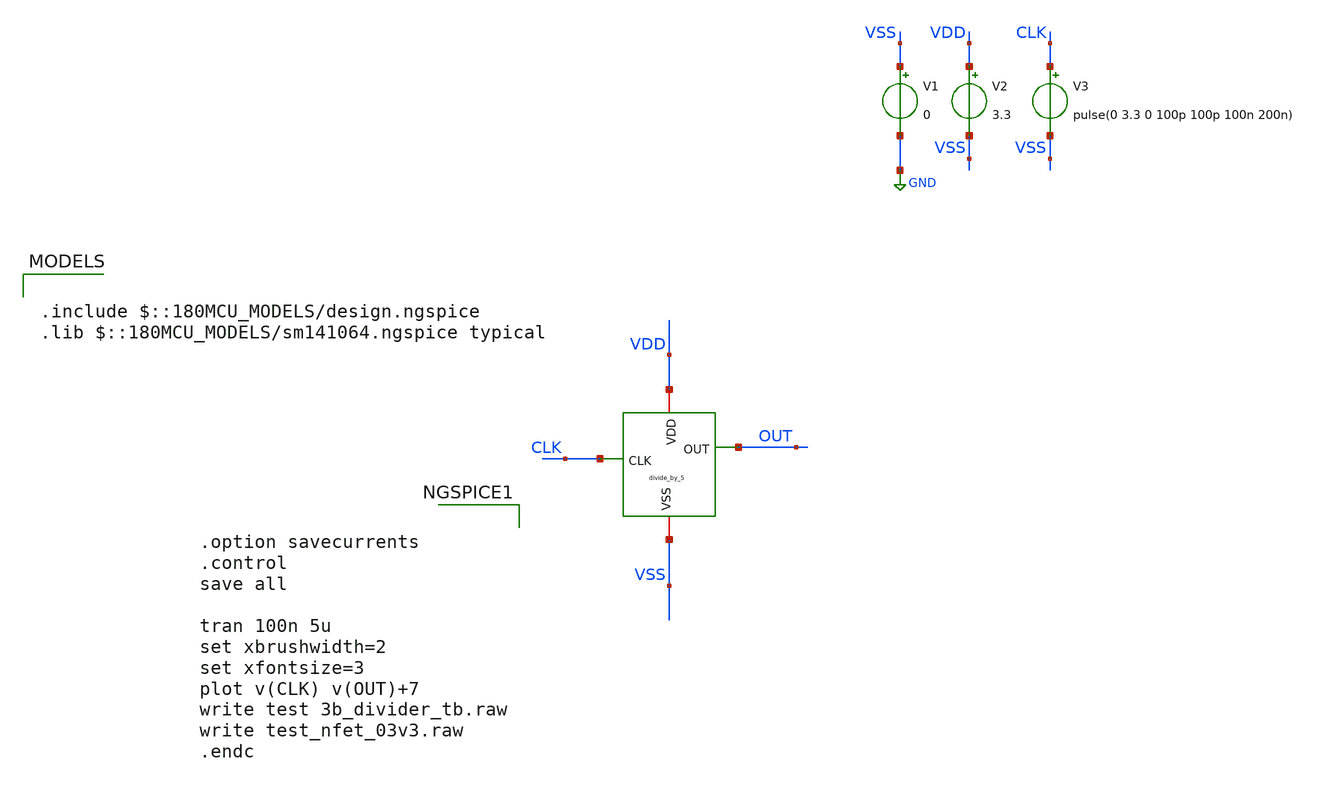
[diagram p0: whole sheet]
** sch_path: Clock_Generator_PAKISTAN_06/Schematics/divide_by_5_tb.sch
**.subckt divide_by_5_tb
x1 VDD CLK OUT VSS divide_by_5
V1 VSS GND 0
V2 VDD VSS 3.3
V3 CLK VSS pulse(0 3.3 0 100p 100p 100n 200n)
**** begin user architecture code

.include $::180MCU_MODELS/design.ngspice
.lib $::180MCU_MODELS/sm141064.ngspice typical



.option savecurrents
.control
save all

tran 100n 5u
set xbrushwidth=2
set xfontsize=3
plot v(CLK) v(OUT)+7
write test 3b_divider_tb.raw
write test_nfet_03v3.raw
.endc


**** end user architecture code
**.ends
.GLOBAL GND
.end
